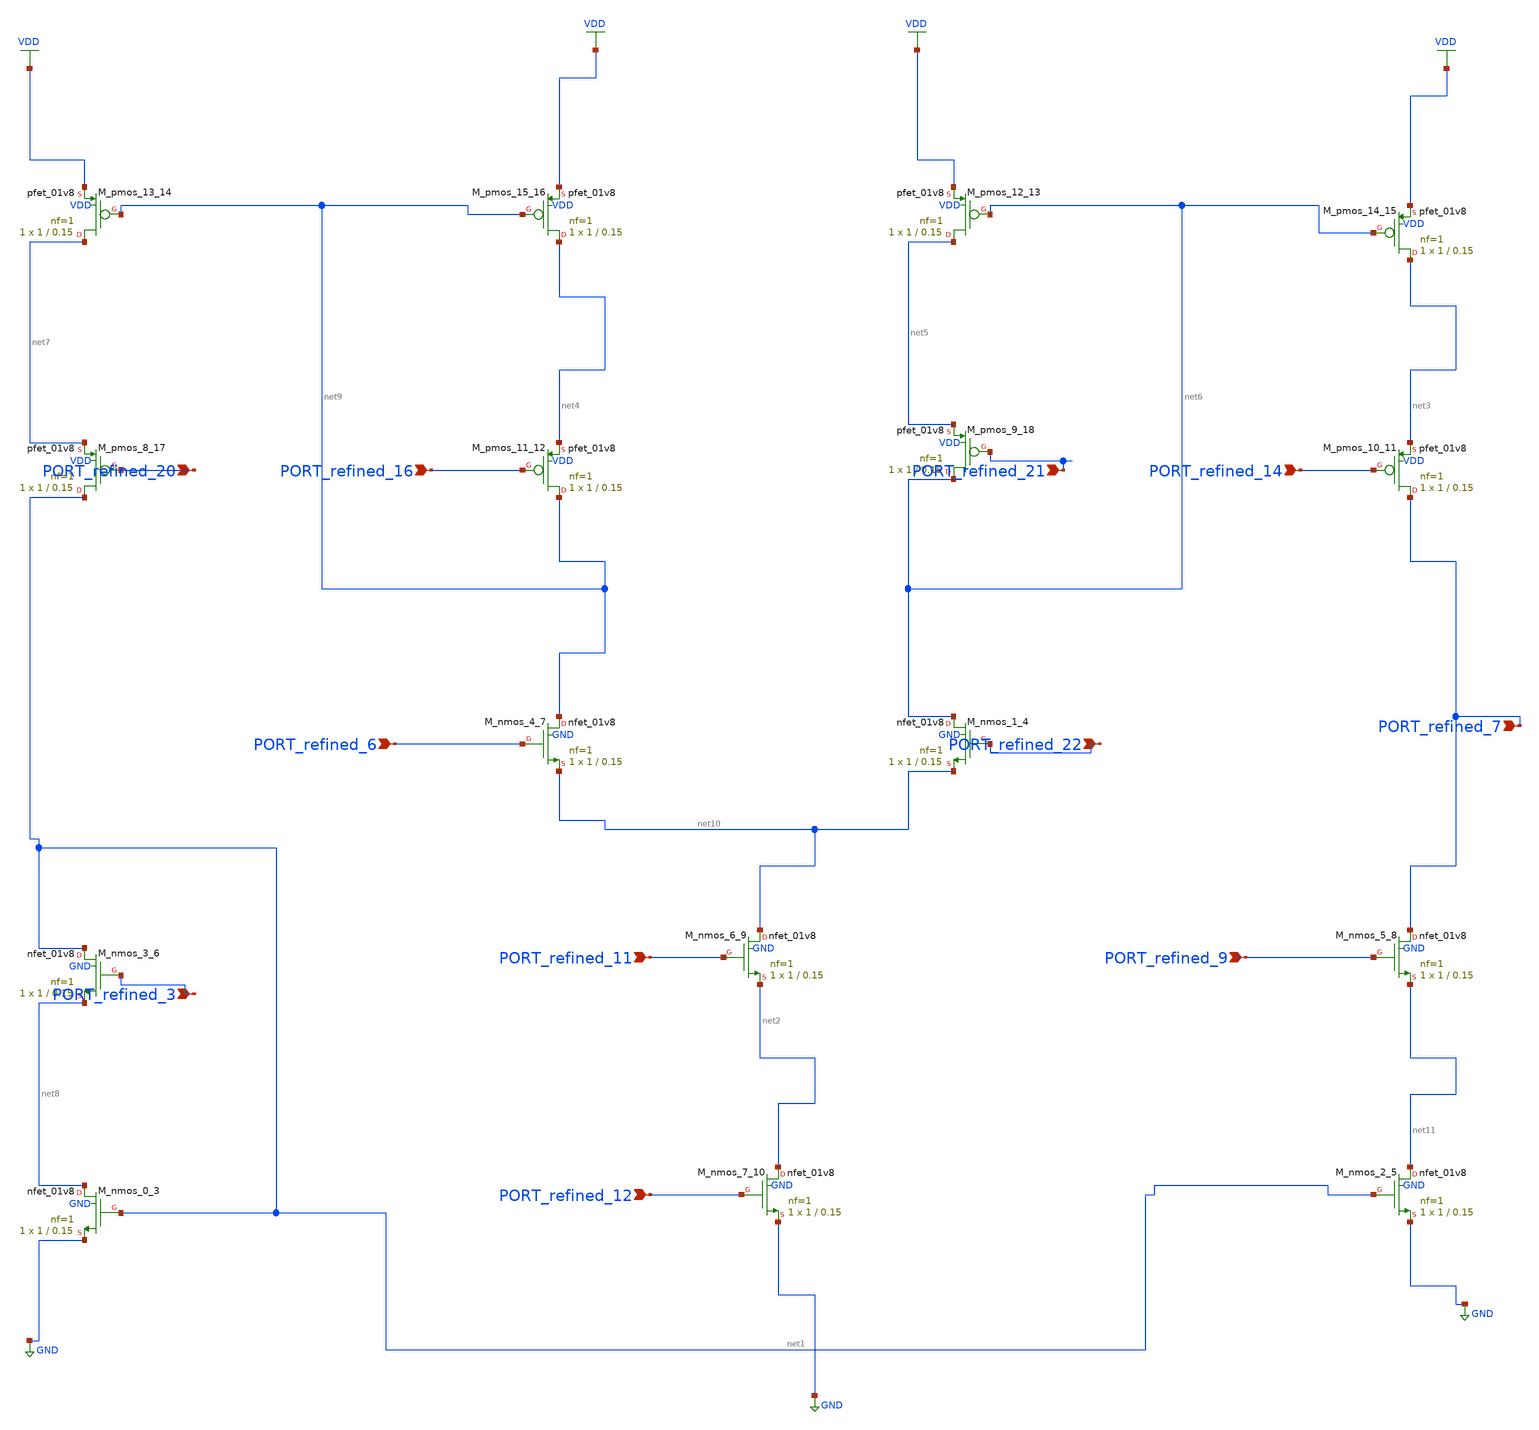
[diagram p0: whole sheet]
** sch_path: schematics/10_1109_ACCESS_2022_3156890_04_002.sch
**.subckt 10_1109_ACCESS_2022_3156890_04_002 PORT_refined_7 PORT_refined_12 PORT_refined_9
*+ PORT_refined_11 PORT_refined_3 PORT_refined_21 PORT_refined_16 PORT_refined_20 PORT_refined_22 PORT_refined_14
*+ PORT_refined_6
*.ipin PORT_refined_7
*.ipin PORT_refined_12
*.ipin PORT_refined_9
*.ipin PORT_refined_11
*.ipin PORT_refined_3
*.ipin PORT_refined_21
*.ipin PORT_refined_16
*.ipin PORT_refined_20
*.ipin PORT_refined_22
*.ipin PORT_refined_14
*.ipin PORT_refined_6
XM_nmos_0_3 net8 net1 GND GND sky130_fd_pr__nfet_01v8 L=0.15 W=1 nf=1 ad='int((1 + 1)/2) * 1 / 1 * 0.29'
+ as='int((1 + 2)/2) * 1 / 1 * 0.29' pd='2*int((1 + 1)/2) * (1 / 1 + 0.29)' ps='2*int((1 + 2)/2) * (1 / 1 + 0.29)'
+ nrd='0.29 / 1 ' nrs='0.29 / 1 ' sa=0 sb=0 sd=0 mult=1 m=1
XM_nmos_1_4 net6 PORT_refined_22 net10 GND sky130_fd_pr__nfet_01v8 L=0.15 W=1 nf=1 ad='int((1 + 1)/2) * 1 / 1 * 0.29'
+ as='int((1 + 2)/2) * 1 / 1 * 0.29' pd='2*int((1 + 1)/2) * (1 / 1 + 0.29)' ps='2*int((1 + 2)/2) * (1 / 1 + 0.29)'
+ nrd='0.29 / 1 ' nrs='0.29 / 1 ' sa=0 sb=0 sd=0 mult=1 m=1
XM_nmos_2_5 net11 net1 GND GND sky130_fd_pr__nfet_01v8 L=0.15 W=1 nf=1 ad='int((1 + 1)/2) * 1 / 1 * 0.29'
+ as='int((1 + 2)/2) * 1 / 1 * 0.29' pd='2*int((1 + 1)/2) * (1 / 1 + 0.29)' ps='2*int((1 + 2)/2) * (1 / 1 + 0.29)'
+ nrd='0.29 / 1 ' nrs='0.29 / 1 ' sa=0 sb=0 sd=0 mult=1 m=1
XM_nmos_3_6 net1 PORT_refined_3 net8 GND sky130_fd_pr__nfet_01v8 L=0.15 W=1 nf=1 ad='int((1 + 1)/2) * 1 / 1 * 0.29'
+ as='int((1 + 2)/2) * 1 / 1 * 0.29' pd='2*int((1 + 1)/2) * (1 / 1 + 0.29)' ps='2*int((1 + 2)/2) * (1 / 1 + 0.29)'
+ nrd='0.29 / 1 ' nrs='0.29 / 1 ' sa=0 sb=0 sd=0 mult=1 m=1
XM_nmos_4_7 net9 PORT_refined_6 net10 GND sky130_fd_pr__nfet_01v8 L=0.15 W=1 nf=1 ad='int((1 + 1)/2) * 1 / 1 * 0.29'
+ as='int((1 + 2)/2) * 1 / 1 * 0.29' pd='2*int((1 + 1)/2) * (1 / 1 + 0.29)' ps='2*int((1 + 2)/2) * (1 / 1 + 0.29)'
+ nrd='0.29 / 1 ' nrs='0.29 / 1 ' sa=0 sb=0 sd=0 mult=1 m=1
XM_nmos_5_8 PORT_refined_7 PORT_refined_9 net11 GND sky130_fd_pr__nfet_01v8 L=0.15 W=1 nf=1 ad='int((1 + 1)/2) * 1 / 1 * 0.29'
+ as='int((1 + 2)/2) * 1 / 1 * 0.29' pd='2*int((1 + 1)/2) * (1 / 1 + 0.29)' ps='2*int((1 + 2)/2) * (1 / 1 + 0.29)'
+ nrd='0.29 / 1 ' nrs='0.29 / 1 ' sa=0 sb=0 sd=0 mult=1 m=1
XM_nmos_6_9 net10 PORT_refined_11 net2 GND sky130_fd_pr__nfet_01v8 L=0.15 W=1 nf=1 ad='int((1 + 1)/2) * 1 / 1 * 0.29'
+ as='int((1 + 2)/2) * 1 / 1 * 0.29' pd='2*int((1 + 1)/2) * (1 / 1 + 0.29)' ps='2*int((1 + 2)/2) * (1 / 1 + 0.29)'
+ nrd='0.29 / 1 ' nrs='0.29 / 1 ' sa=0 sb=0 sd=0 mult=1 m=1
XM_nmos_7_10 net2 PORT_refined_12 GND GND sky130_fd_pr__nfet_01v8 L=0.15 W=1 nf=1 ad='int((1 + 1)/2) * 1 / 1 * 0.29'
+ as='int((1 + 2)/2) * 1 / 1 * 0.29' pd='2*int((1 + 1)/2) * (1 / 1 + 0.29)' ps='2*int((1 + 2)/2) * (1 / 1 + 0.29)'
+ nrd='0.29 / 1 ' nrs='0.29 / 1 ' sa=0 sb=0 sd=0 mult=1 m=1
XM_pmos_10_11 PORT_refined_7 PORT_refined_14 net3 VDD sky130_fd_pr__pfet_01v8 L=0.15 W=1 nf=1 ad='int((1 + 1)/2) * 1 / 1 * 0.29'
+ as='int((1 + 2)/2) * 1 / 1 * 0.29' pd='2*int((1 + 1)/2) * (1 / 1 + 0.29)' ps='2*int((1 + 2)/2) * (1 / 1 + 0.29)'
+ nrd='0.29 / 1 ' nrs='0.29 / 1 ' sa=0 sb=0 sd=0 mult=1 m=1
XM_pmos_11_12 net9 PORT_refined_16 net4 VDD sky130_fd_pr__pfet_01v8 L=0.15 W=1 nf=1 ad='int((1 + 1)/2) * 1 / 1 * 0.29'
+ as='int((1 + 2)/2) * 1 / 1 * 0.29' pd='2*int((1 + 1)/2) * (1 / 1 + 0.29)' ps='2*int((1 + 2)/2) * (1 / 1 + 0.29)'
+ nrd='0.29 / 1 ' nrs='0.29 / 1 ' sa=0 sb=0 sd=0 mult=1 m=1
XM_pmos_12_13 net5 net6 VDD VDD sky130_fd_pr__pfet_01v8 L=0.15 W=1 nf=1 ad='int((1 + 1)/2) * 1 / 1 * 0.29'
+ as='int((1 + 2)/2) * 1 / 1 * 0.29' pd='2*int((1 + 1)/2) * (1 / 1 + 0.29)' ps='2*int((1 + 2)/2) * (1 / 1 + 0.29)'
+ nrd='0.29 / 1 ' nrs='0.29 / 1 ' sa=0 sb=0 sd=0 mult=1 m=1
XM_pmos_13_14 net7 net9 VDD VDD sky130_fd_pr__pfet_01v8 L=0.15 W=1 nf=1 ad='int((1 + 1)/2) * 1 / 1 * 0.29'
+ as='int((1 + 2)/2) * 1 / 1 * 0.29' pd='2*int((1 + 1)/2) * (1 / 1 + 0.29)' ps='2*int((1 + 2)/2) * (1 / 1 + 0.29)'
+ nrd='0.29 / 1 ' nrs='0.29 / 1 ' sa=0 sb=0 sd=0 mult=1 m=1
XM_pmos_14_15 net3 net6 VDD VDD sky130_fd_pr__pfet_01v8 L=0.15 W=1 nf=1 ad='int((1 + 1)/2) * 1 / 1 * 0.29'
+ as='int((1 + 2)/2) * 1 / 1 * 0.29' pd='2*int((1 + 1)/2) * (1 / 1 + 0.29)' ps='2*int((1 + 2)/2) * (1 / 1 + 0.29)'
+ nrd='0.29 / 1 ' nrs='0.29 / 1 ' sa=0 sb=0 sd=0 mult=1 m=1
XM_pmos_15_16 net4 net9 VDD VDD sky130_fd_pr__pfet_01v8 L=0.15 W=1 nf=1 ad='int((1 + 1)/2) * 1 / 1 * 0.29'
+ as='int((1 + 2)/2) * 1 / 1 * 0.29' pd='2*int((1 + 1)/2) * (1 / 1 + 0.29)' ps='2*int((1 + 2)/2) * (1 / 1 + 0.29)'
+ nrd='0.29 / 1 ' nrs='0.29 / 1 ' sa=0 sb=0 sd=0 mult=1 m=1
XM_pmos_8_17 net1 PORT_refined_20 net7 VDD sky130_fd_pr__pfet_01v8 L=0.15 W=1 nf=1 ad='int((1 + 1)/2) * 1 / 1 * 0.29'
+ as='int((1 + 2)/2) * 1 / 1 * 0.29' pd='2*int((1 + 1)/2) * (1 / 1 + 0.29)' ps='2*int((1 + 2)/2) * (1 / 1 + 0.29)'
+ nrd='0.29 / 1 ' nrs='0.29 / 1 ' sa=0 sb=0 sd=0 mult=1 m=1
XM_pmos_9_18 net6 PORT_refined_21 net5 VDD sky130_fd_pr__pfet_01v8 L=0.15 W=1 nf=1 ad='int((1 + 1)/2) * 1 / 1 * 0.29'
+ as='int((1 + 2)/2) * 1 / 1 * 0.29' pd='2*int((1 + 1)/2) * (1 / 1 + 0.29)' ps='2*int((1 + 2)/2) * (1 / 1 + 0.29)'
+ nrd='0.29 / 1 ' nrs='0.29 / 1 ' sa=0 sb=0 sd=0 mult=1 m=1
**.ends
.GLOBAL GND
.GLOBAL VDD
.end
